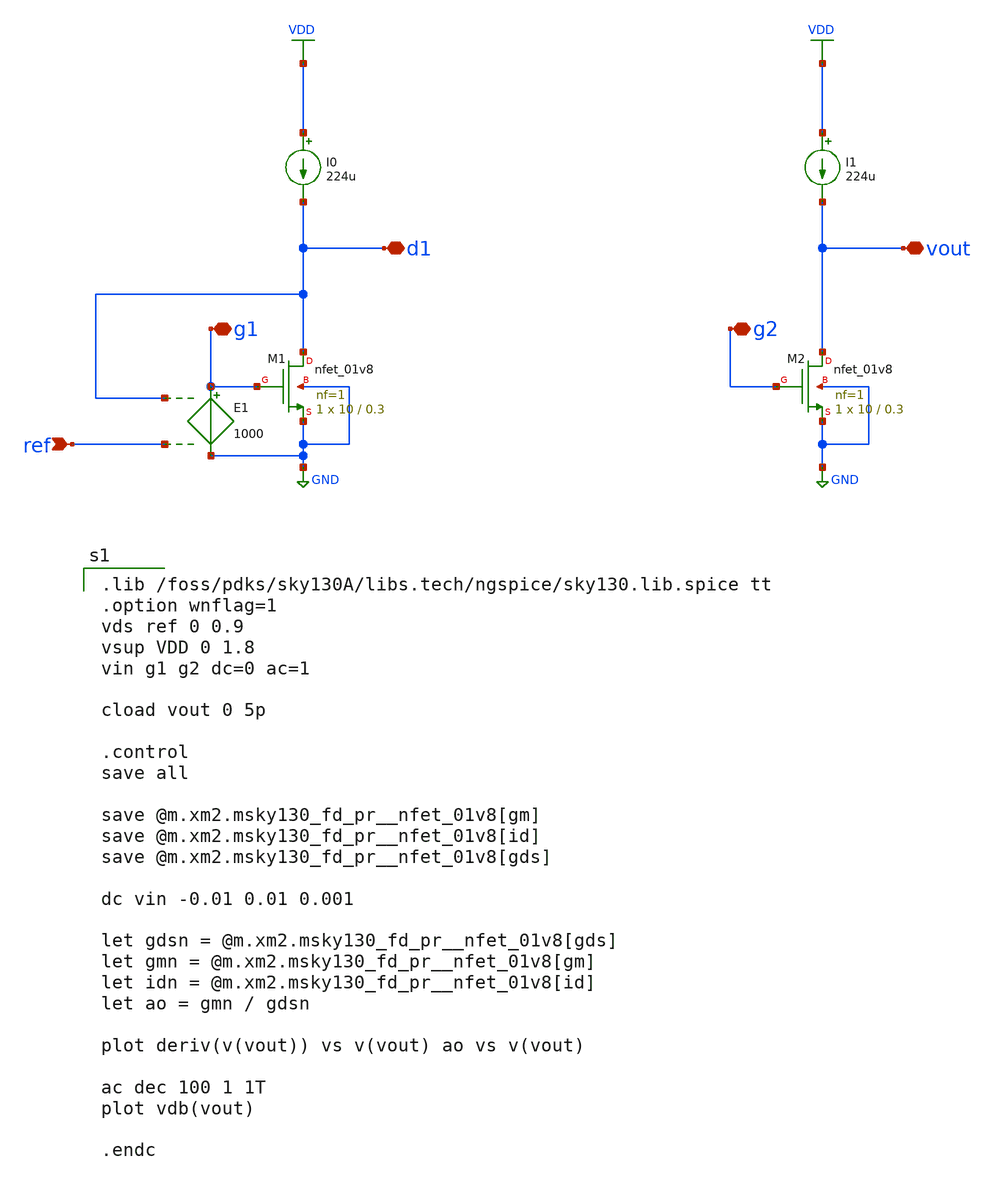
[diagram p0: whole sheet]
** sch_path: cs_amp_full_IPD413HW1.sch
**.subckt cs_amp_full_IPD413HW1 ref g1 d1 g2 vout
*.ipin ref
*.iopin g1
*.iopin d1
*.iopin g2
*.iopin vout
E1 g1 GND d1 ref 1000
I0 VDD d1 224u
I1 VDD vout 224u
XM1 d1 g1 GND GND sky130_fd_pr__nfet_01v8 L=0.3 W=10 nf=1 ad='int((nf+1)/2) * W/nf * 0.29' as='int((nf+2)/2) * W/nf * 0.29'
+ pd='2*int((nf+1)/2) * (W/nf + 0.29)' ps='2*int((nf+2)/2) * (W/nf + 0.29)' nrd='0.29 / W' nrs='0.29 / W'
+ sa=0 sb=0 sd=0 mult=1 m=1
XM2 vout g2 GND GND sky130_fd_pr__nfet_01v8 L=0.3 W=10 nf=1 ad='int((nf+1)/2) * W/nf * 0.29' as='int((nf+2)/2) * W/nf * 0.29'
+ pd='2*int((nf+1)/2) * (W/nf + 0.29)' ps='2*int((nf+2)/2) * (W/nf + 0.29)' nrd='0.29 / W' nrs='0.29 / W'
+ sa=0 sb=0 sd=0 mult=1 m=1
**** begin user architecture code

.lib /foss/pdks/sky130A/libs.tech/ngspice/sky130.lib.spice tt
.option wnflag=1
vds ref 0 0.9
vsup VDD 0 1.8
vin g1 g2 dc=0 ac=1

cload vout 0 5p

.control
save all

save @m.xm2.msky130_fd_pr__nfet_01v8[gm]
save @m.xm2.msky130_fd_pr__nfet_01v8[id]
save @m.xm2.msky130_fd_pr__nfet_01v8[gds]

dc vin -0.01 0.01 0.001

let gdsn = @m.xm2.msky130_fd_pr__nfet_01v8[gds]
let gmn = @m.xm2.msky130_fd_pr__nfet_01v8[gm]
let idn = @m.xm2.msky130_fd_pr__nfet_01v8[id]
let ao = gmn / gdsn

plot deriv(v(vout)) vs v(vout) ao vs v(vout)

ac dec 100 1 1T
plot vdb(vout)

.endc

**** end user architecture code
**.ends
.GLOBAL GND
.GLOBAL VDD
.end
